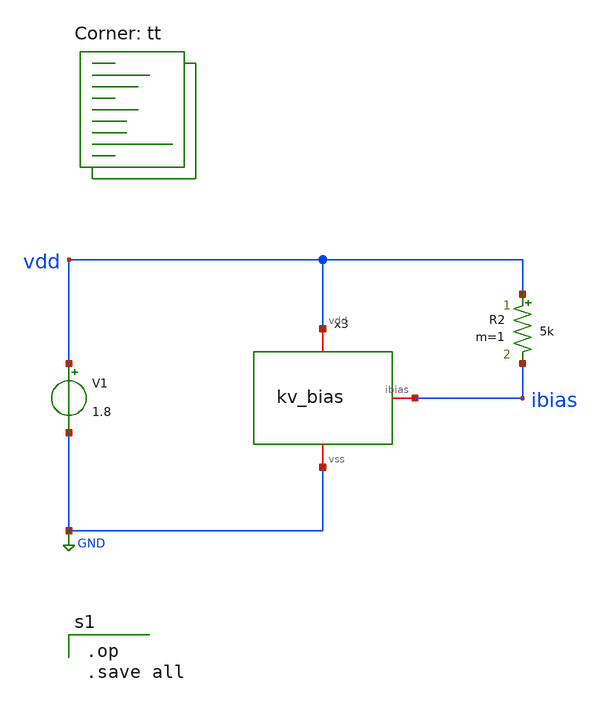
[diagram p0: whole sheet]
** sch_path: examples/demo_tapeout/xschem/tb_bias.sch
**.subckt tb_bias
V1 vdd GND 1.8
x3 vdd GND ibias kv_bias
R2 vdd ibias 5k m=1
**** begin user architecture code
.lib $::SKYWATER_MODELS/sky130.lib.spice tt

.op
.save all

**** end user architecture code
**.ends

* expanding   symbol:  kv_bias.sym # of pins=3
** sym_path: examples/demo_tapeout/xschem/kv_bias.sym
** sch_path: examples/demo_tapeout/xschem/kv_bias.sch
.subckt kv_bias vdd vss ibias
*.iopin vdd
*.iopin vss
*.iopin ibias
R1 vdd nb 10k m=1
XM1 nb nb vss vss sky130_fd_pr__nfet_01v8 L=1u W=2u nf=1 ad='int((1 + 1)/2) * 2u / 1 * 0.29' as='int((1 + 2)/2) * 2u / 1 * 0.29'
+ pd='2*int((1 + 1)/2) * (2u / 1 + 0.29)' ps='2*int((1 + 2)/2) * (2u / 1 + 0.29)' nrd='0.29 / 2u ' nrs='0.29 / 2u '
+ sa=0 sb=0 sd=0 mult=1 m=1
XM2 ibias nb vss vss sky130_fd_pr__nfet_01v8 L=1u W=2u nf=1 ad='int((1 + 1)/2) * 2u / 1 * 0.29' as='int((1 + 2)/2) * 2u / 1 * 0.29'
+ pd='2*int((1 + 1)/2) * (2u / 1 + 0.29)' ps='2*int((1 + 2)/2) * (2u / 1 + 0.29)' nrd='0.29 / 2u ' nrs='0.29 / 2u '
+ sa=0 sb=0 sd=0 mult=1 m=1
.ends

.GLOBAL GND
.end
